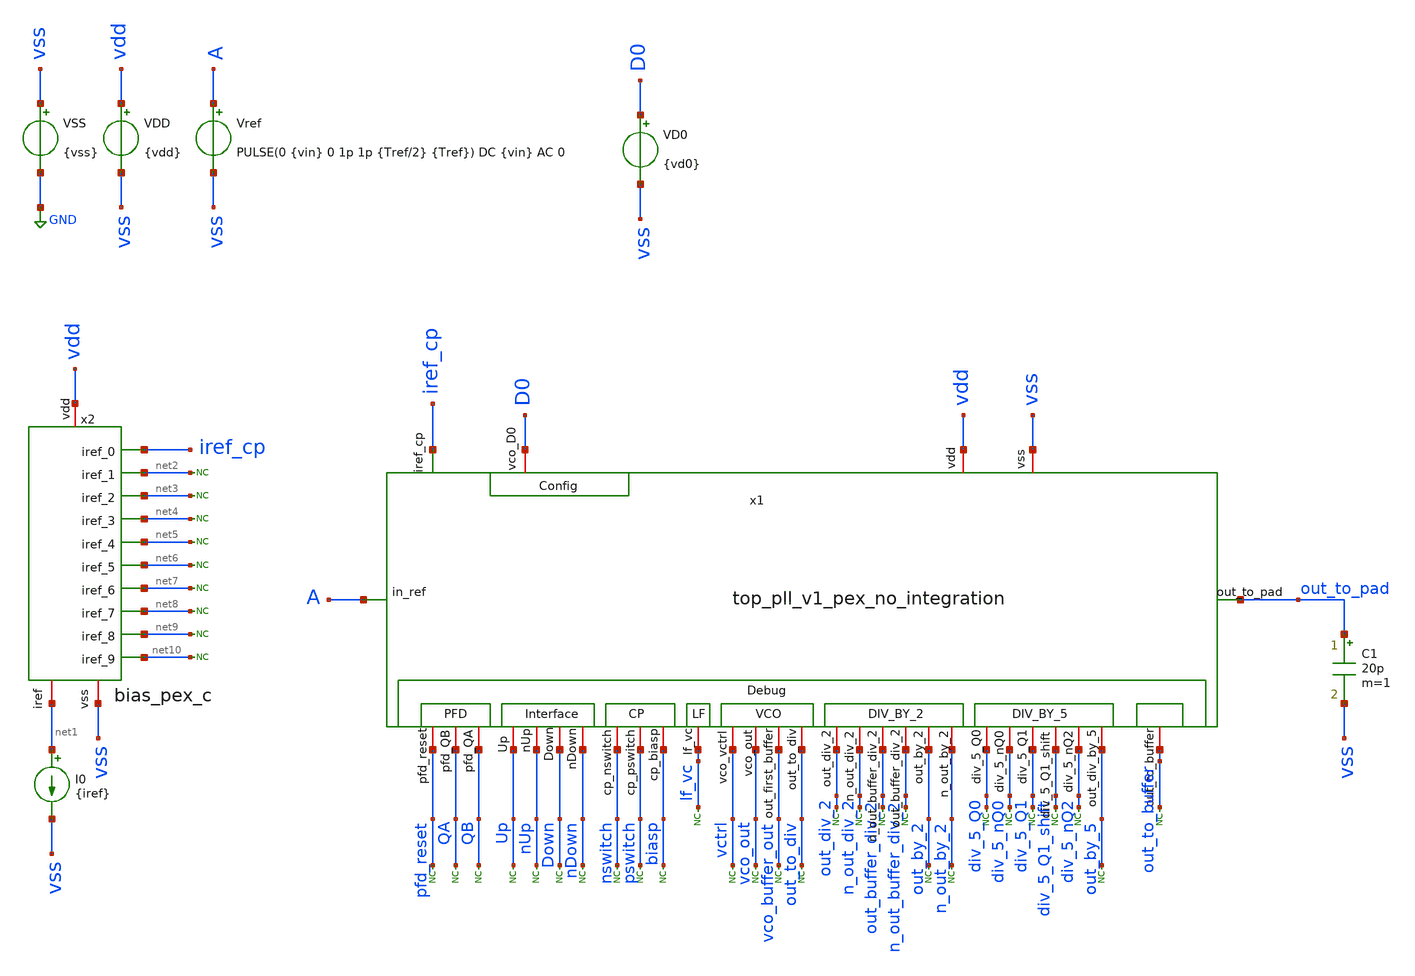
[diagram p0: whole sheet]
** sch_path: xschem/tb_top_pll_v1_pex_no_integration.sch
**.subckt tb_top_pll_v1_pex_no_integration
VSS vss GND {vss}
VDD vdd vss {vdd}
Vref A vss PULSE(0 {vin} 0 1p 1p {Tref/2} {Tref}) DC {vin} AC 0
VD0 D0 vss {vd0}
I0 net1 vss {iref}
* noconn #net2
* noconn #net3
* noconn #net4
* noconn #net5
* noconn #net6
* noconn #net7
* noconn #net8
* noconn #net9
* noconn #net10
* noconn div_5_nQ2
* noconn div_5_Q1_shift
* noconn div_5_Q1
* noconn div_5_nQ0
* noconn div_5_Q0
* noconn n_out_buffer_div_2
* noconn out_buffer_div_2
* noconn n_out_div_2
* noconn out_div_2
* noconn nswitch
* noconn pswitch
* noconn biasp
* noconn pfd_reset
* noconn QA
* noconn QB
* noconn Up
* noconn nUp
* noconn Down
* noconn nDown
* noconn lf_vc
* noconn vctrl
* noconn vco_out
* noconn vco_buffer_out
* noconn out_to_div
* noconn out_by_2
* noconn n_out_by_2
* noconn out_by_5
x2 vdd net1 vss iref_cp net2 net3 net4 net5 net6 net7 net8 net9 net10 bias_pex_c
x1 iref_cp vss vdd vco_out vctrl Up QB nUp A out_to_pad Down nDown QA D0 lf_vc vco_buffer_out biasp
+ pswitch pfd_reset nswitch out_by_2 out_to_div out_by_5 n_out_by_2 div_5_nQ0 div_5_Q1_shift div_5_Q1
+ out_buffer_div_2 n_out_buffer_div_2 div_5_Q0 n_out_div_2 div_5_nQ2 out_div_2 out_to_buffer
+ top_pll_v1_pex_no_integration
C1 out_to_pad vss 20p m=1
* noconn out_to_buffer
**** begin user architecture code



* Parameters
.param kp = 1.0
.param vdd = kp*1.8
.param vss = 0.0
.param vin = vdd
.param fref = 100e6
.param Tref = 1/fref
.param iref = 100u
.param vd0 = 0.0

.options TEMP = 100.0
.options RSHUNT = 1e20

* Models
.lib ~/skywater/skywater-pdk/libraries/sky130_fd_pr_ngspice/latest/models/corners/sky130.lib SS
.include ~/caravel_analog_fulgor/xschem/simulations/PFD_pex_c.spice
.include ~/caravel_analog_fulgor/xschem/simulations/pfd_cp_interface_pex_c.spice
.include ~/caravel_analog_fulgor/xschem/simulations/charge_pump_pex_c.spice
.include ~/caravel_analog_fulgor/xschem/simulations/loop_filter_pex_c.spice
.include ~/caravel_analog_fulgor/xschem/simulations/csvco_pex_c.spice
.include ~/caravel_analog_fulgor/xschem/simulations/ring_osc_buffer_pex_c.spice
.include ~/caravel_analog_fulgor/xschem/simulations/div_by_2_pex_c.spice
.include ~/caravel_analog_fulgor/xschem/simulations/div_by_5_pex_c.spice
.include ~/caravel_analog_fulgor/xschem/simulations/bias_pex_c.spice
.include ~/caravel_analog_fulgor/xschem/simulations/buffer_salida_pex_c.spice

* Data to save

.ic v(A) = 0.0
.ic v(QA) = 0.0
.ic v(QB) = 0.0
.ic v(Up) = 0.0
.ic v(nUp) = 0.0
.ic v(Down) = 0.0
.ic v(nDown) = 0.0
.ic v(vctrl) = 0.0
.ic v(D0) = 0.0
.ic v(vco_out) = 0.0
.ic v(vco_buffer_out) = 0.0
.ic v(out_to_div) = 0.0
.ic v(out_to_pad) = 0.0
.ic v(out_div_2) = 0.0
.ic v(n_out_div_2) = 0.0
.ic v(out_buffer_div_2) = 0.0
.ic v(n_out_buffer_div_2) = 0.0
.ic v(out_by_2) = 0.0
.ic v(n_out_by_2) = 0.0
.ic v(div_5_Q0) = 0.0
.ic v(div_5_nQ0) = 0.0
.ic v(div_5_Q1) = 0.0
.ic v(div_5_Q1_shift) = 0.0
.ic v(div_5_nQ2) = 0.0
.ic v(out_by_5) = 0.0

* Simulation
.control
	tran 0.01ns 1.5us
	meas tran Tosc trig v(out_to_pad) val=0.9 fall=1005 targ v(out_to_pad) val=0.9 fall=1105
	let  T = Tosc/100.0
	let  f = 1/T
	echo .
	echo ------ PLL simulation ------
	print T f
	*write tb_PLL_tran.raw
	plot v(vctrl) v(pfd_reset)+2 v(nDown)+4 v(Down)+6 v(nUp)+8 v(Up)+10 v(QA)+12 v(QB)+12 v(A)+14
+ v(out_by_5)+16
 	plot v(out_to_pad)+9 v(out_to_div)+6 v(out_by_2)+3 v(out_by_5)
	plot v(out_by_5) v(out_by_2) v(out_to_div)
	plot v(vctrl)
	plot v(pswitch) v(nswitch) xlimit 1.4us 1.444us
.endc

.end


**** end user architecture code
**.ends
.GLOBAL GND
**** begin user architecture code
[sky130_models]
**** end user architecture code
.end
